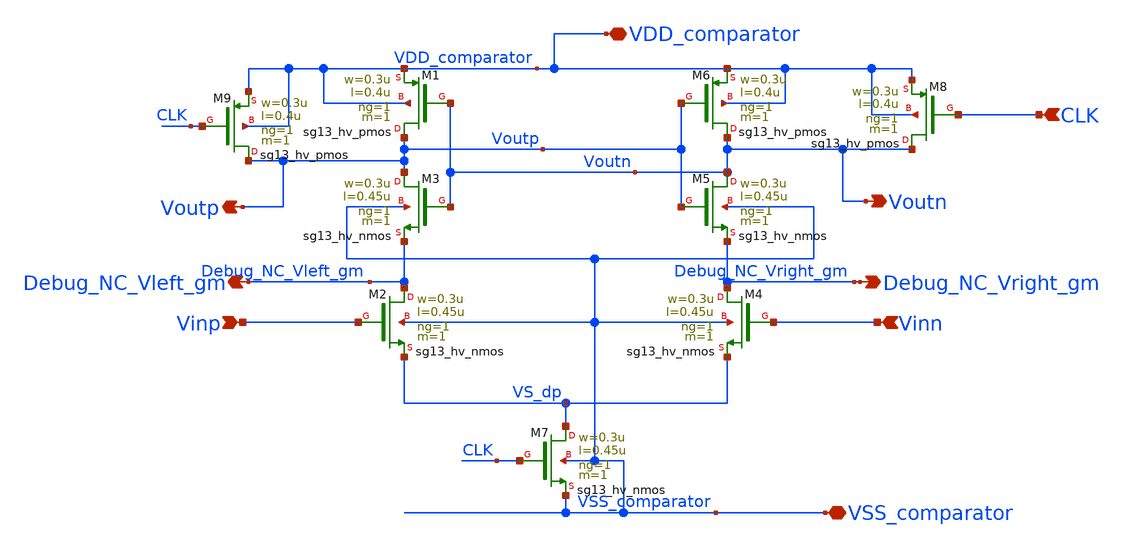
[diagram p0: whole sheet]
** sch_path: circuit_files/xschem_symbols/simple_comparator.sch
**.subckt simple_comparator CLK Vinp VSS_comparator VDD_comparator Vinn Debug_NC_Vright_gm
*+ Debug_NC_Vleft_gm Voutp Voutn
*.ipin CLK
*.ipin Vinp
*.iopin VSS_comparator
*.iopin VDD_comparator
*.ipin Vinn
*.opin Debug_NC_Vright_gm
*.opin Debug_NC_Vleft_gm
*.opin Voutp
*.opin Voutn
XM1 Voutp Voutn VDD_comparator VDD_comparator sg13_hv_pmos w=0.3u l=0.4u ng=1 m=1 mm_ok=1
XM2 Debug_NC_Vleft_gm Vinp VS_dp VSS_comparator sg13_hv_nmos w=0.3u l=0.45u ng=1 m=1 mm_ok=1
XM3 Voutp Voutn Debug_NC_Vleft_gm VSS_comparator sg13_hv_nmos w=0.3u l=0.45u ng=1 m=1 mm_ok=1
XM4 Debug_NC_Vright_gm Vinn VS_dp VSS_comparator sg13_hv_nmos w=0.3u l=0.45u ng=1 m=1 mm_ok=1
XM5 Voutn Voutp Debug_NC_Vright_gm VSS_comparator sg13_hv_nmos w=0.3u l=0.45u ng=1 m=1 mm_ok=1
XM6 Voutn Voutp VDD_comparator VDD_comparator sg13_hv_pmos w=0.3u l=0.4u ng=1 m=1 mm_ok=1
XM7 VS_dp CLK VSS_comparator VSS_comparator sg13_hv_nmos w=0.3u l=0.45u ng=1 m=1 mm_ok=1
XM8 Voutn CLK VDD_comparator VDD_comparator sg13_hv_pmos w=0.3u l=0.4u ng=1 m=1 mm_ok=1
XM9 Voutp CLK VDD_comparator VDD_comparator sg13_hv_pmos w=0.3u l=0.4u ng=1 m=1 mm_ok=1
**.ends
.end
